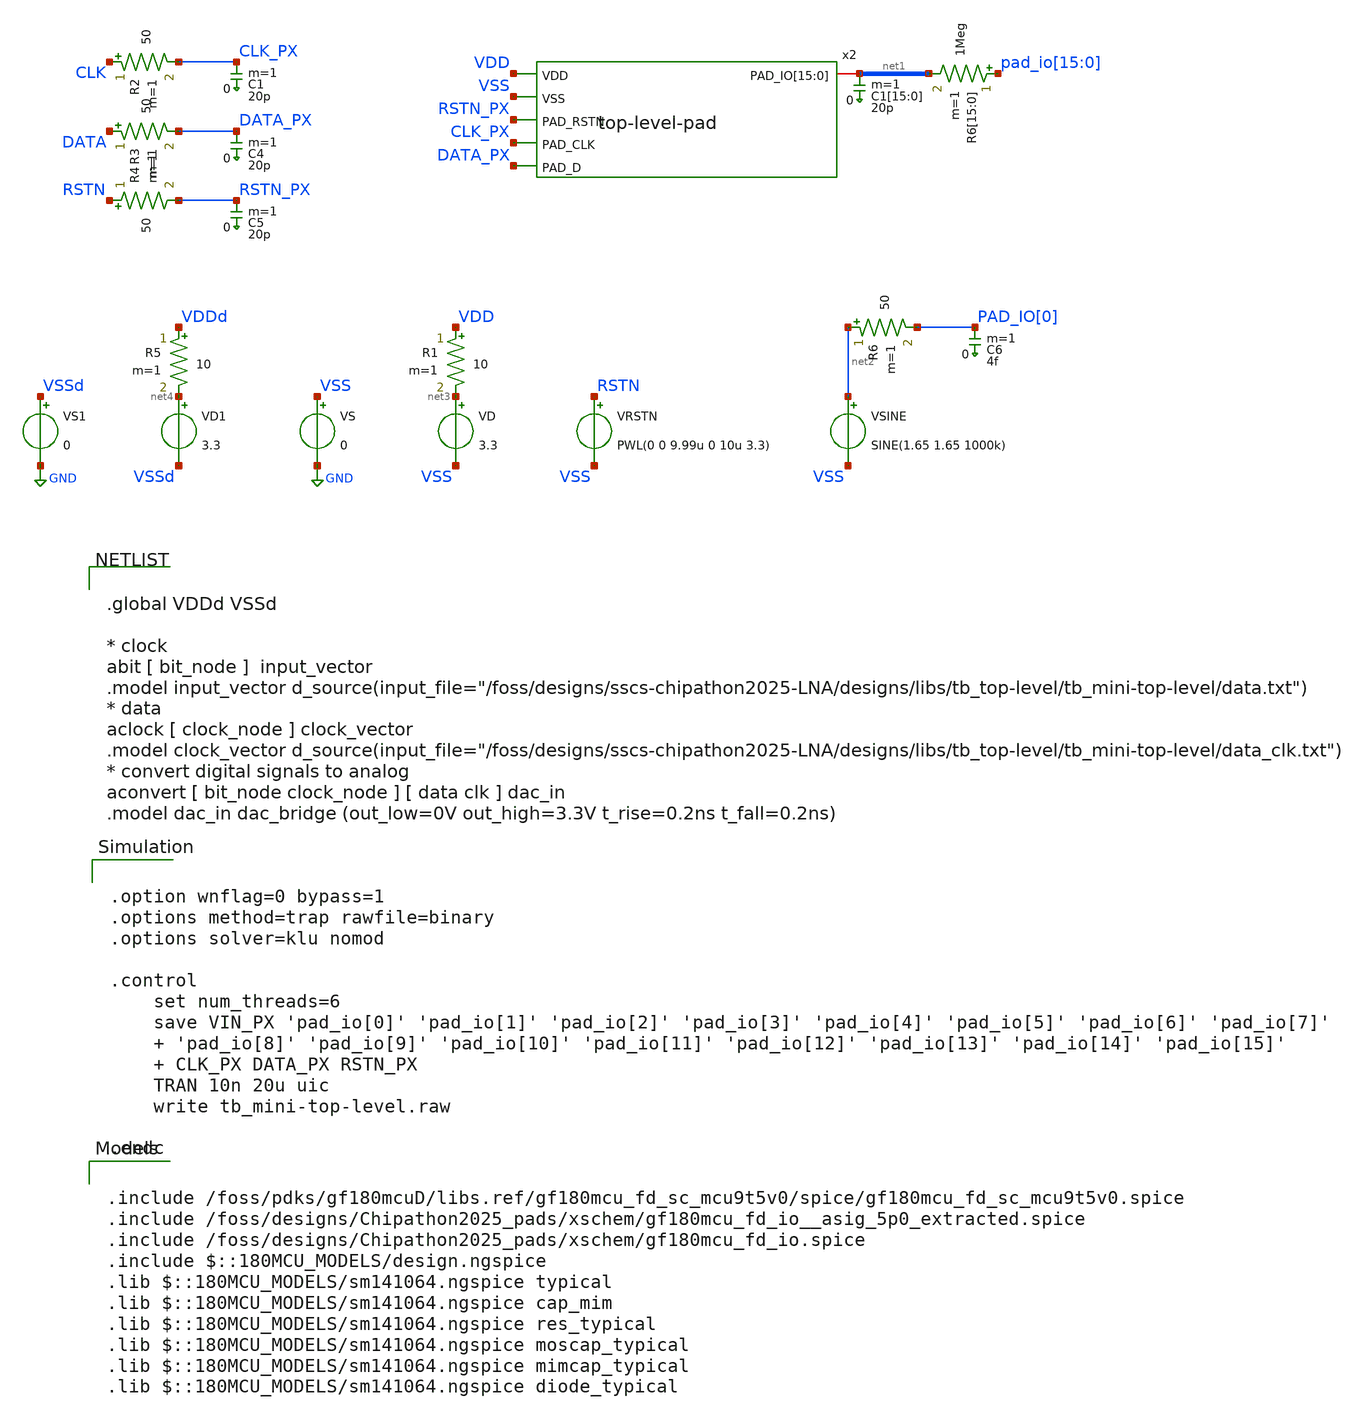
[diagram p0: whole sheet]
** sch_path: designs/libs/tb_top-level/tb_full-top-level/tb_full-top-level.sch
**.subckt tb_full-top-level
VD net3 VSS 3.3
R1 VDD net3 10 m=1
R2 CLK CLK_PX 50 m=1
R3 DATA DATA_PX 50 m=1
VS VSS GND 0
VRSTN RSTN VSS PWL(0 0 9.99u 0 10u 3.3)
R4 RSTN RSTN_PX 50 m=1
VD1 net4 VSSd 3.3
R5 VDDd net4 10 m=1
VS1 VSSd GND 0
C1[15] net1[15] 0 20p m=1
C1[14] net1[14] 0 20p m=1
C1[13] net1[13] 0 20p m=1
C1[12] net1[12] 0 20p m=1
C1[11] net1[11] 0 20p m=1
C1[10] net1[10] 0 20p m=1
C1[9] net1[9] 0 20p m=1
C1[8] net1[8] 0 20p m=1
C1[7] net1[7] 0 20p m=1
C1[6] net1[6] 0 20p m=1
C1[5] net1[5] 0 20p m=1
C1[4] net1[4] 0 20p m=1
C1[3] net1[3] 0 20p m=1
C1[2] net1[2] 0 20p m=1
C1[1] net1[1] 0 20p m=1
C1[0] net1[0] 0 20p m=1
C1 CLK_PX 0 20p m=1
C4 DATA_PX 0 20p m=1
R6[15] pad_io[15] net1[15] 1Meg m=1
R6[14] pad_io[14] net1[14] 1Meg m=1
R6[13] pad_io[13] net1[13] 1Meg m=1
R6[12] pad_io[12] net1[12] 1Meg m=1
R6[11] pad_io[11] net1[11] 1Meg m=1
R6[10] pad_io[10] net1[10] 1Meg m=1
R6[9] pad_io[9] net1[9] 1Meg m=1
R6[8] pad_io[8] net1[8] 1Meg m=1
R6[7] pad_io[7] net1[7] 1Meg m=1
R6[6] pad_io[6] net1[6] 1Meg m=1
R6[5] pad_io[5] net1[5] 1Meg m=1
R6[4] pad_io[4] net1[4] 1Meg m=1
R6[3] pad_io[3] net1[3] 1Meg m=1
R6[2] pad_io[2] net1[2] 1Meg m=1
R6[1] pad_io[1] net1[1] 1Meg m=1
R6[0] pad_io[0] net1[0] 1Meg m=1
C5 RSTN_PX 0 20p m=1
VSINE net2 VSS SINE(1.65 1.65 1000k)
R6 net2 PAD_IO[0] 50 m=1
C6 PAD_IO[0] 0 4f m=1
x2 VDD VSS RSTN_PX CLK_PX DATA_PX net1[15] net1[14] net1[13] net1[12] net1[11] net1[10] net1[9]
+ net1[8] net1[7] net1[6] net1[5] net1[4] net1[3] net1[2] net1[1] net1[0] top-level-pad
**** begin user architecture code


.option wnflag=0 bypass=1
.options method=trap rawfile=binary
.options solver=klu nomod

.control
    set num_threads=6
    save VIN_PX 'pad_io[0]' 'pad_io[1]' 'pad_io[2]' 'pad_io[3]' 'pad_io[4]' 'pad_io[5]' 'pad_io[6]' 'pad_io[7]'
    + 'pad_io[8]' 'pad_io[9]' 'pad_io[10]' 'pad_io[11]' 'pad_io[12]' 'pad_io[13]' 'pad_io[14]' 'pad_io[15]'
    + CLK_PX DATA_PX RSTN_PX
    TRAN 10n 20u uic
    write tb_mini-top-level.raw

.endc



.include /foss/pdks/gf180mcuD/libs.ref/gf180mcu_fd_sc_mcu9t5v0/spice/gf180mcu_fd_sc_mcu9t5v0.spice
.include /foss/designs/Chipathon2025_pads/xschem/gf180mcu_fd_io__asig_5p0_extracted.spice
.include /foss/designs/Chipathon2025_pads/xschem/gf180mcu_fd_io.spice
.include $::180MCU_MODELS/design.ngspice
.lib $::180MCU_MODELS/sm141064.ngspice typical
.lib $::180MCU_MODELS/sm141064.ngspice cap_mim
.lib $::180MCU_MODELS/sm141064.ngspice res_typical
.lib $::180MCU_MODELS/sm141064.ngspice moscap_typical
.lib $::180MCU_MODELS/sm141064.ngspice mimcap_typical
.lib $::180MCU_MODELS/sm141064.ngspice diode_typical



.global VDDd VSSd

* clock
abit [ bit_node ]  input_vector
.model input_vector
+ d_source(input_file="/foss/designs/sscs-chipathon2025-LNA/designs/libs/tb_top-level/tb_mini-top-level/data.txt")
* data
aclock [ clock_node ] clock_vector
.model clock_vector
+ d_source(input_file="/foss/designs/sscs-chipathon2025-LNA/designs/libs/tb_top-level/tb_mini-top-level/data_clk.txt")
* convert digital signals to analog
aconvert [ bit_node clock_node ] [ data clk ] dac_in
.model dac_in dac_bridge (out_low=0V out_high=3.3V t_rise=0.2ns t_fall=0.2ns)


**** end user architecture code
**.ends
.GLOBAL GND
.end
